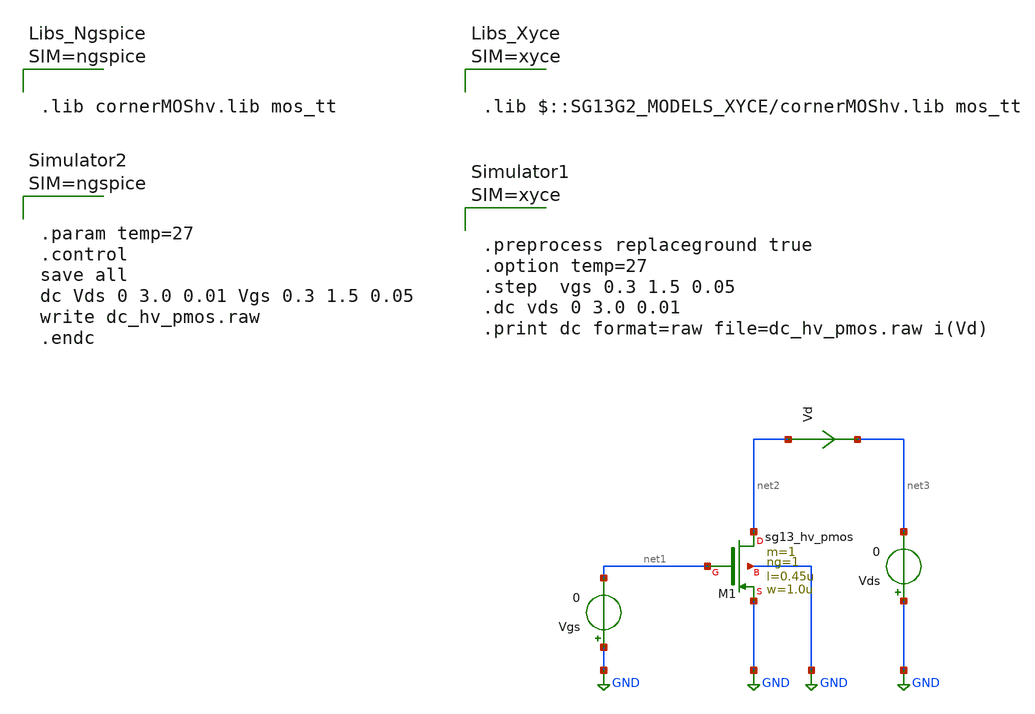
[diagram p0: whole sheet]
** sch_path: ihp-sg13g2/libs.tech/xschem/sg13g2_tests_xyce/dc_hv_pmos.sch
* Copyright 2023 IHP PDK Authors
**.subckt dc_hv_pmos
Vgs GND net1 0
Vds GND net3 0
XM1 net2 net1 GND GND sg13_hv_pmos w=1.0u l=0.45u ng=1 m=1 mm_ok=1
Vd net2 net3 0
.save i(vd)
**** begin user architecture code









.lib cornerMOShv.lib mos_tt






.param temp=27
.control
save all
dc Vds 0 3.0 0.01 Vgs 0.3 1.5 0.05
write dc_hv_pmos.raw
.endc



**** end user architecture code
**.ends
.GLOBAL GND
.end
